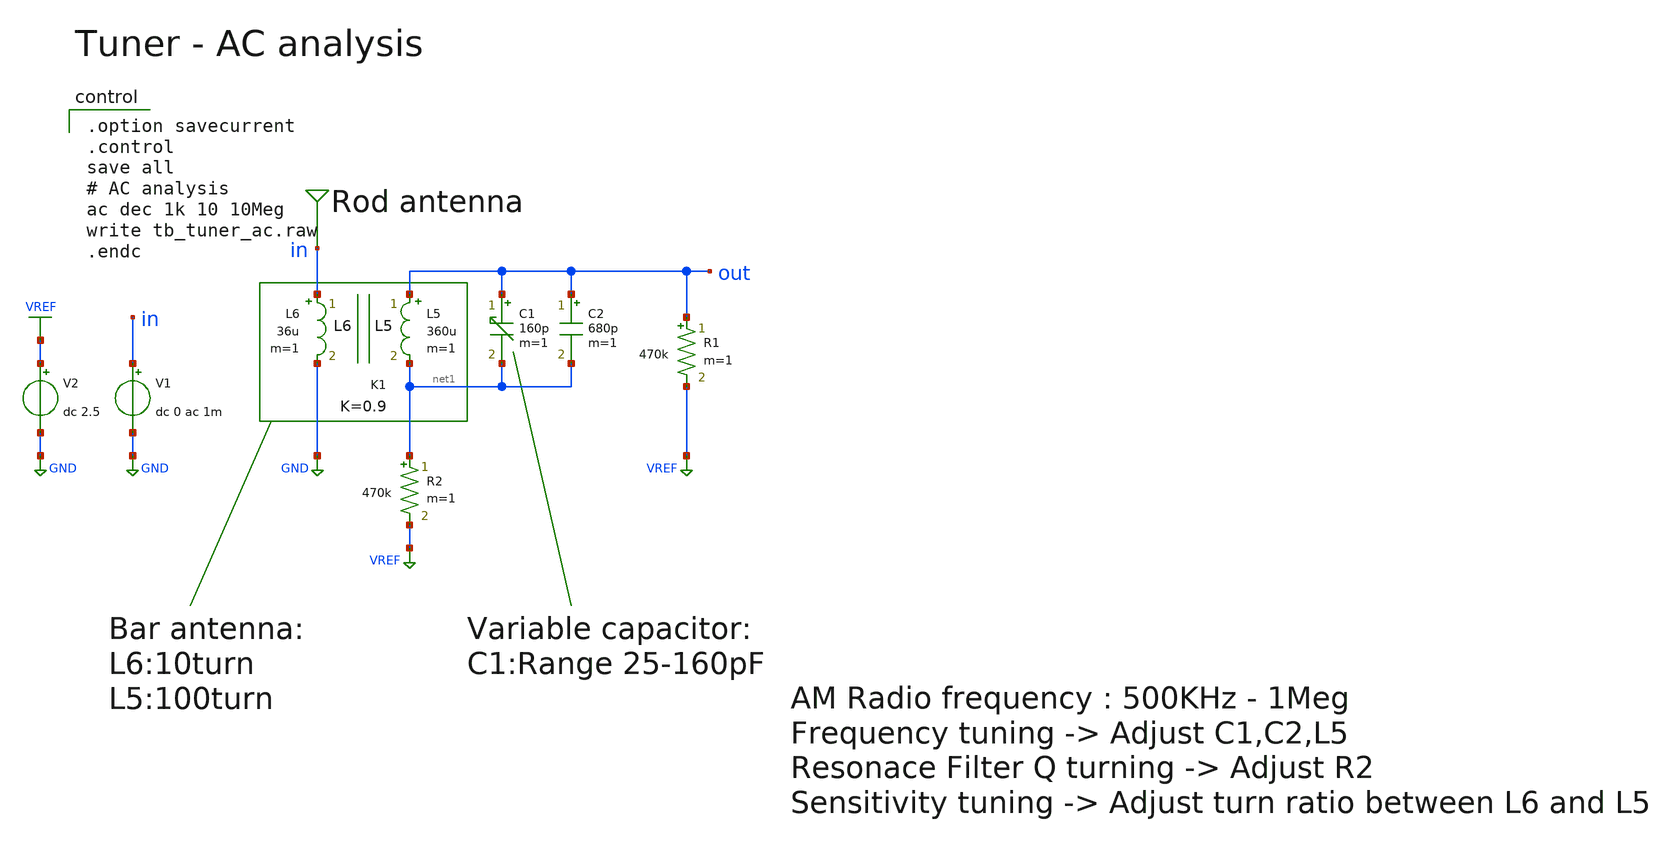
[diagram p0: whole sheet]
** sch_path: member_project/AM_Radio/Yamada3/xschem/tb_tuner_ac.sch
**.subckt tb_tuner_ac
V1 in GND dc 0 ac 1m
C1 out net1 160p m=1
L6 in GND 36u m=1
K1 L5 L6 0.9
L5 out net1 360u m=1
R1 out VREF 470k m=1
R2 net1 VREF 470k m=1
C2 out net1 680p m=1
V2 VREF GND dc 2.5
**** begin user architecture code

.option savecurrent
.control
save all
# AC analysis
ac dec 1k 10 10Meg
write tb_tuner_ac.raw
.endc

**** end user architecture code
**.ends
.GLOBAL GND
.GLOBAL VREF
.end
